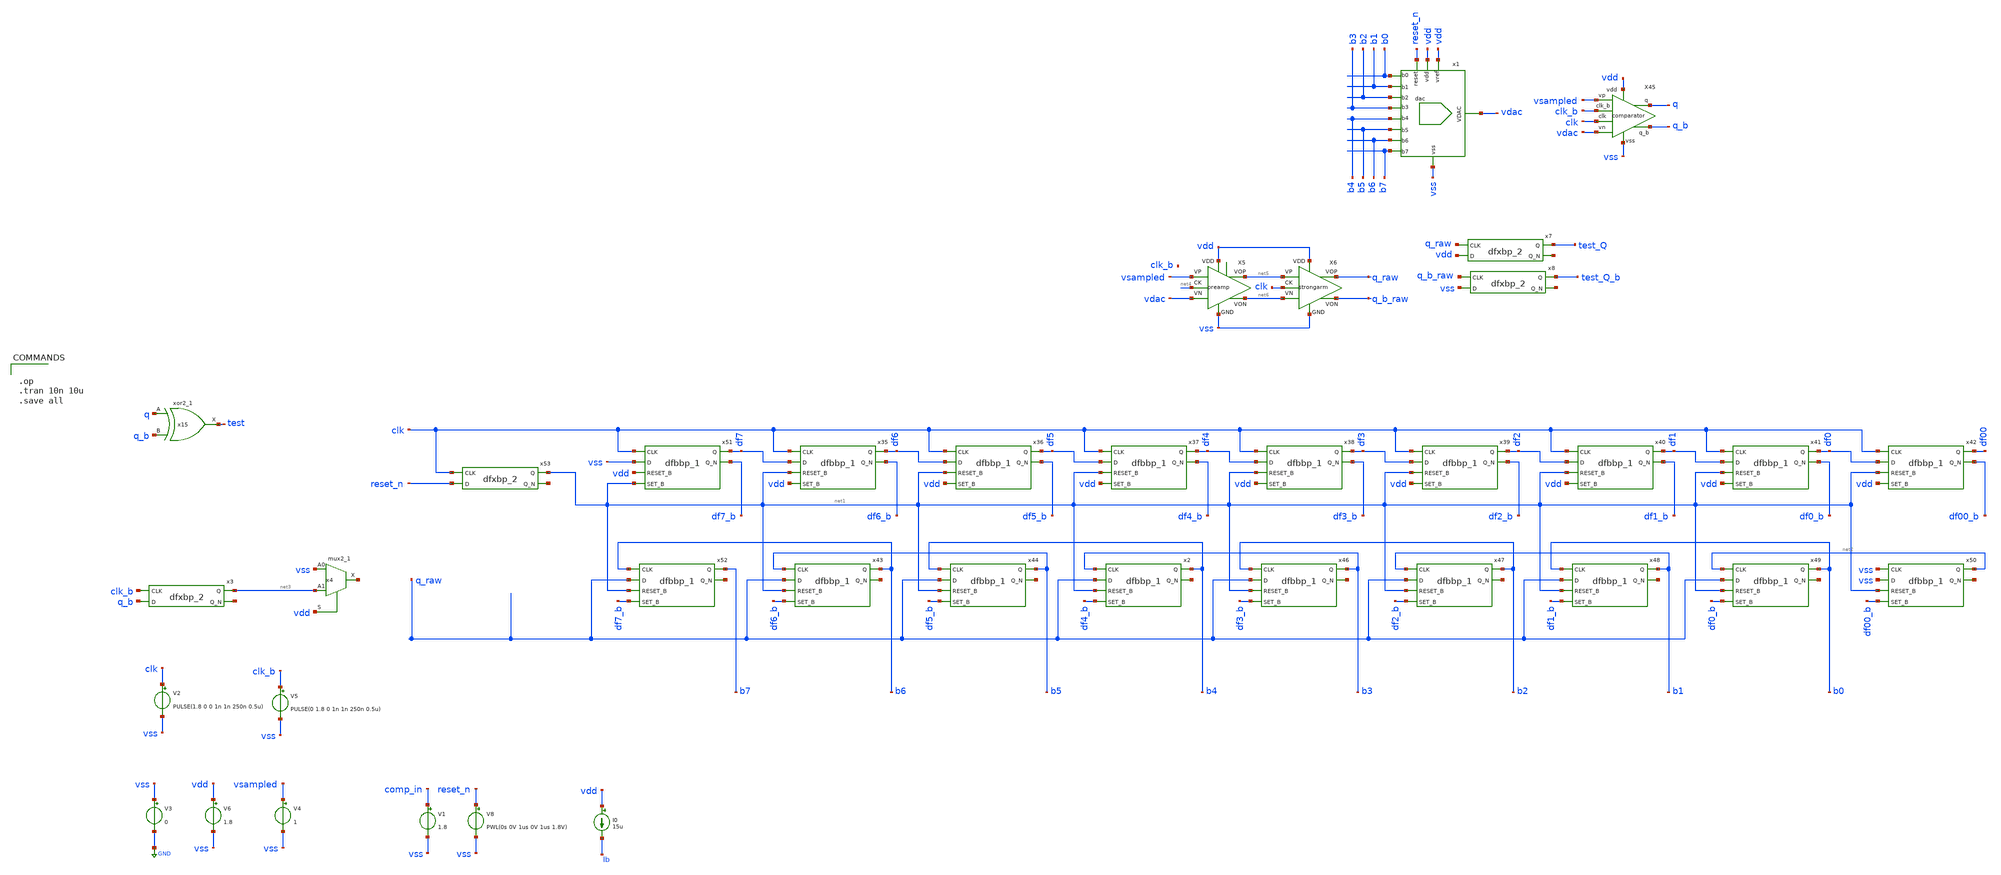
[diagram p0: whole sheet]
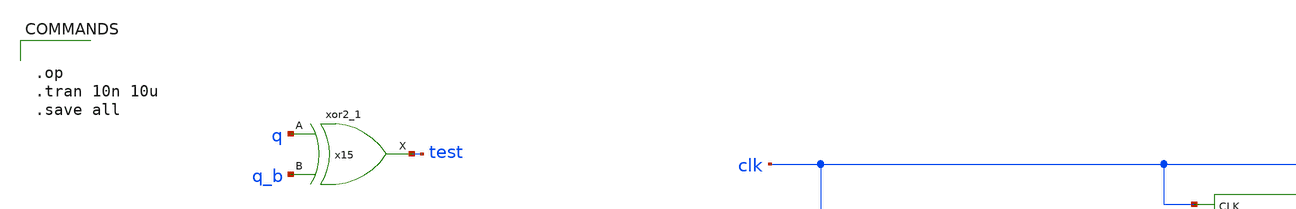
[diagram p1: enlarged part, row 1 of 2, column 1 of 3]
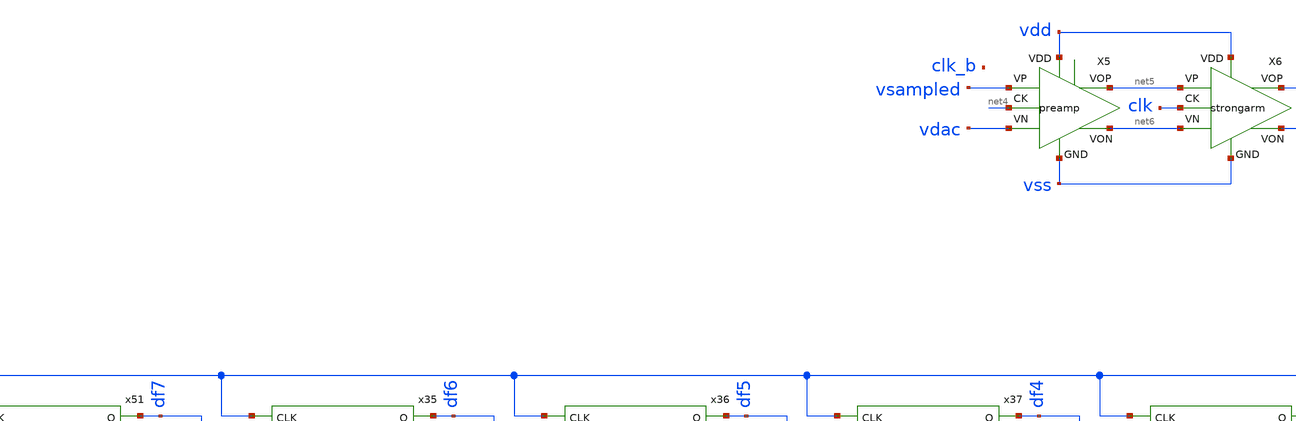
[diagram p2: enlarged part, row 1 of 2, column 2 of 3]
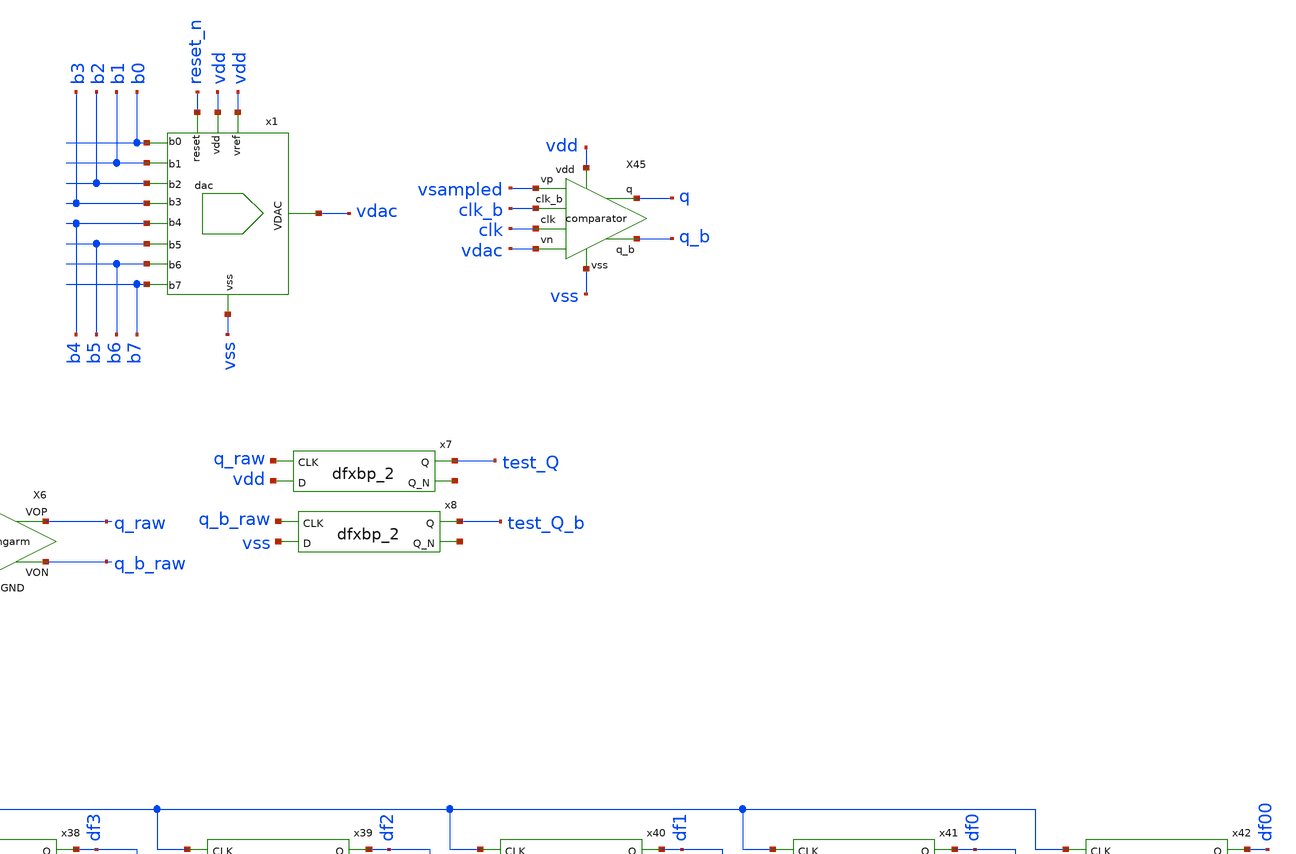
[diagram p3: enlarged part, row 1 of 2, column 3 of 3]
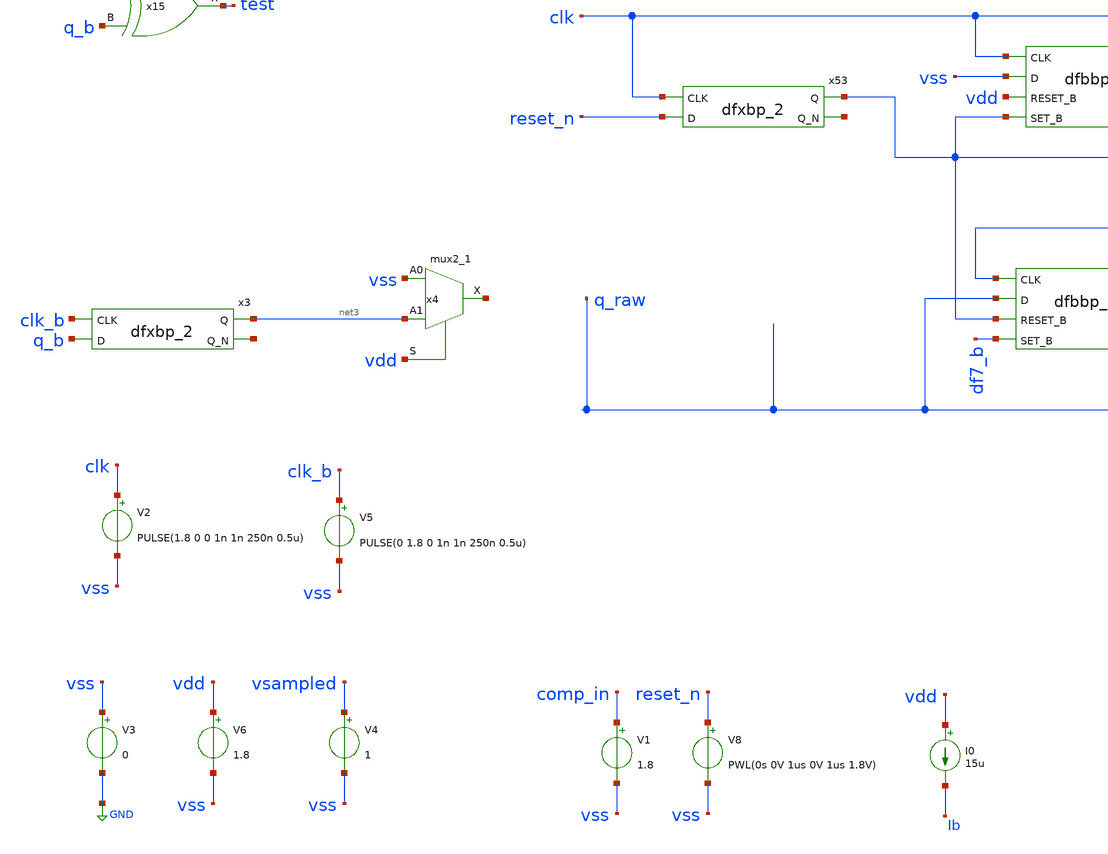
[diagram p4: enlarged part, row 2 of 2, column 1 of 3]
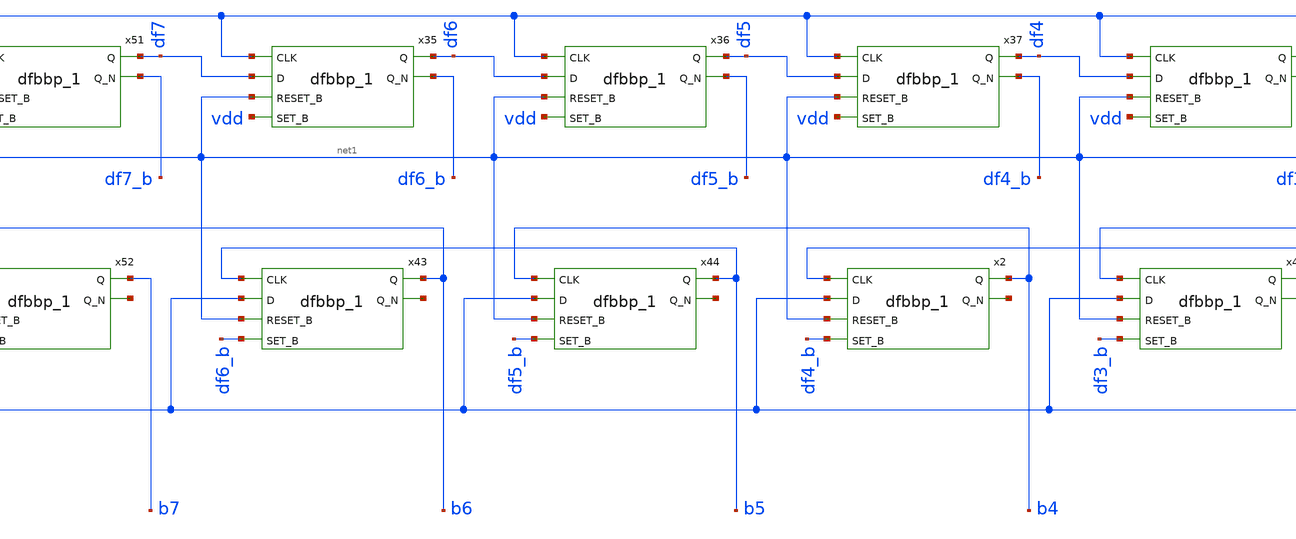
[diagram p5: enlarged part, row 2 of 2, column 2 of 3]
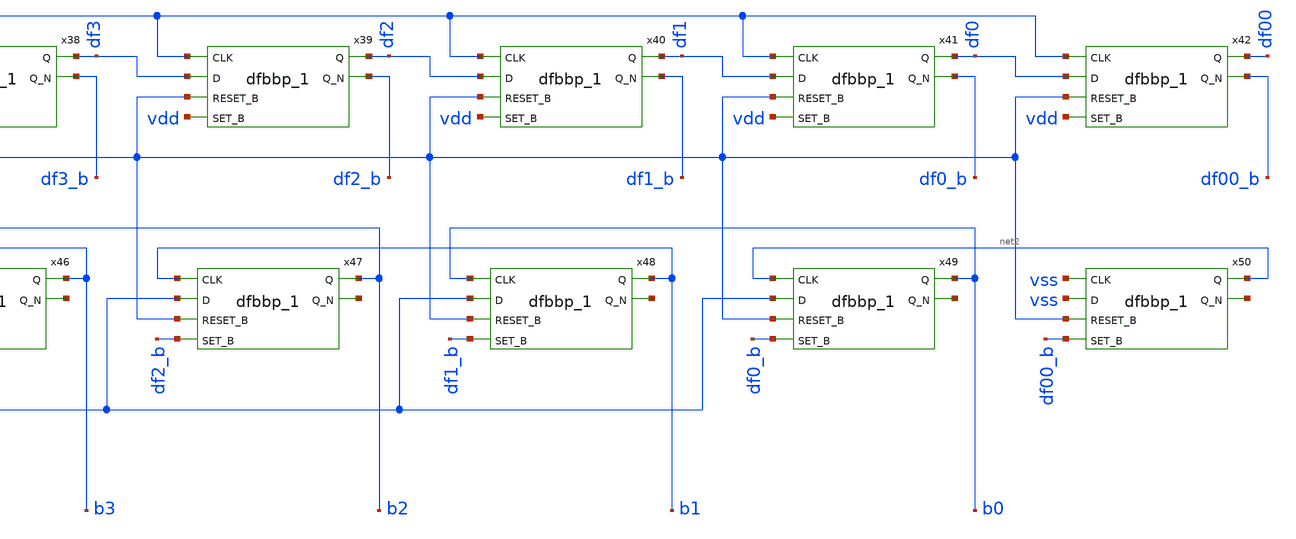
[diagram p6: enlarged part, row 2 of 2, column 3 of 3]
** sch_path: xschem/sar_logic/sar_logic_tb.sch
.lib $::SKYWATER_MODELS/sky130.lib.spice tt
.include $::SKYWATER_STDCELLS/sky130_fd_sc_hd.spice

**.subckt sar_logic_tb
V2 clk vss PULSE(1.8 0 0 1n 1n 250n 0.5u)
V1 comp_in vss 1.8
V6 vdd vss 1.8
V8 reset_n vss PWL(0s 0V 1us 0V 1us 1.8V)
I0 vdd Ib 15u
x1 vss vdac vdd vdd b0 b1 b2 b3 b4 b5 b6 b7 reset_n dac
V3 vss GND 0
V5 clk_b vss PULSE(0 1.8 0 1n 1n 250n 0.5u)
X45 vsampled vdac vss q_b q vdd clk clk_b comparator
V4 vsampled vss 1
x35 clk df7 net1 vdd vss vss vdd vdd df6 df6_b sky130_fd_sc_hd__dfbbp_1
x36 clk df6 net1 vdd vss vss vdd vdd df5 df5_b sky130_fd_sc_hd__dfbbp_1
x37 clk df5 net1 vdd vss vss vdd vdd df4 df4_b sky130_fd_sc_hd__dfbbp_1
x38 clk df4 net1 vdd vss vss vdd vdd df3 df3_b sky130_fd_sc_hd__dfbbp_1
x39 clk df3 net1 vdd vss vss vdd vdd df2 df2_b sky130_fd_sc_hd__dfbbp_1
x40 clk df2 net1 vdd vss vss vdd vdd df1 df1_b sky130_fd_sc_hd__dfbbp_1
x41 clk df1 net1 vdd vss vss vdd vdd df0 df0_b sky130_fd_sc_hd__dfbbp_1
x42 clk df0 net1 vdd vss vss vdd vdd df00 df00_b sky130_fd_sc_hd__dfbbp_1
x43 b5 q_raw net1 df6_b vss vss vdd vdd b6 net7 sky130_fd_sc_hd__dfbbp_1
x44 b4 q_raw net1 df5_b vss vss vdd vdd b5 net8 sky130_fd_sc_hd__dfbbp_1
x2 b3 q_raw net1 df4_b vss vss vdd vdd b4 net9 sky130_fd_sc_hd__dfbbp_1
x46 b2 q_raw net1 df3_b vss vss vdd vdd b3 net10 sky130_fd_sc_hd__dfbbp_1
x47 b1 q_raw net1 df2_b vss vss vdd vdd b2 net11 sky130_fd_sc_hd__dfbbp_1
x48 b0 q_raw net1 df1_b vss vss vdd vdd b1 net12 sky130_fd_sc_hd__dfbbp_1
x49 net2 q_raw net1 df0_b vss vss vdd vdd b0 net13 sky130_fd_sc_hd__dfbbp_1
x50 vss vss net1 df00_b vss vss vdd vdd net2 net14 sky130_fd_sc_hd__dfbbp_1
x51 clk vss vdd net1 vss vss vdd vdd df7 df7_b sky130_fd_sc_hd__dfbbp_1
x52 b6 q_raw net1 df7_b vss vss vdd vdd b7 net15 sky130_fd_sc_hd__dfbbp_1
x53 clk reset_n vss vss vdd vdd net1 net16 sky130_fd_sc_hd__dfxbp_2
x3 clk_b q_b vss vss vdd vdd net3 net17 sky130_fd_sc_hd__dfxbp_2
x4 vss net3 vdd vss vss vdd vdd net18 sky130_fd_sc_hd__mux2_1
x15 q q_b vss vss vdd vdd test sky130_fd_sc_hd__xor2_1
X5 vsampled vdac vss net6 net5 vdd net4 preamp
X6 net5 net6 vss q_b_raw q_raw vdd clk strongarm
x7 q_raw vdd vss vss vdd vdd test_Q net19 sky130_fd_sc_hd__dfxbp_2
x8 q_b_raw vss vss vss vdd vdd test_Q_b net20 sky130_fd_sc_hd__dfxbp_2
**** begin user architecture code


.op
.tran 10n 10u
.save all


**** end user architecture code
**.ends
.GLOBAL GND
.end
